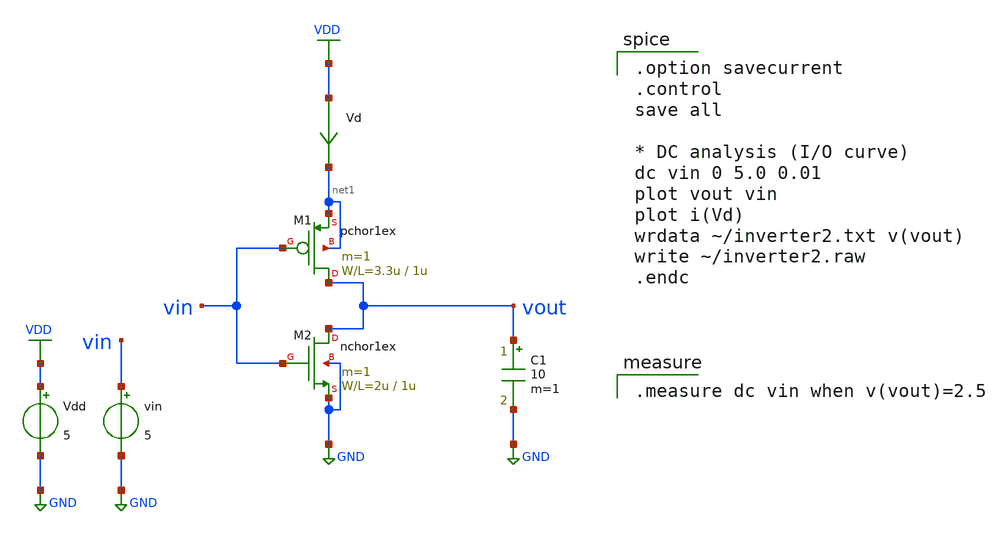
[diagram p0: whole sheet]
** sch_path: member_project/hiro-ogawa/others/inverter2.sch
**.subckt inverter2
Vdd VDD GND 5
vin vin GND 5
Vd VDD net1 0
.save i(vd)
C1 vout GND 10 m=1
M1 vout vin net1 net1 pchor1ex L=1u W=3.3u m=1
M2 vout vin GND GND nchor1ex L=1u W=2u m=1
**** begin user architecture code
 .include $::LIB/mos.lib
.include $::LIB/passive.lib
.include $::LIB/diode.lib

.option savecurrent
.control
save all

* DC analysis (I/O curve)
dc vin 0 5.0 0.01
plot vout vin
plot i(Vd)
wrdata ~/inverter2.txt v(vout)
write ~/inverter2.raw
.endc



.measure dc vin when v(vout)=2.5

**** end user architecture code
**.ends
.GLOBAL VDD
.GLOBAL GND
.end
